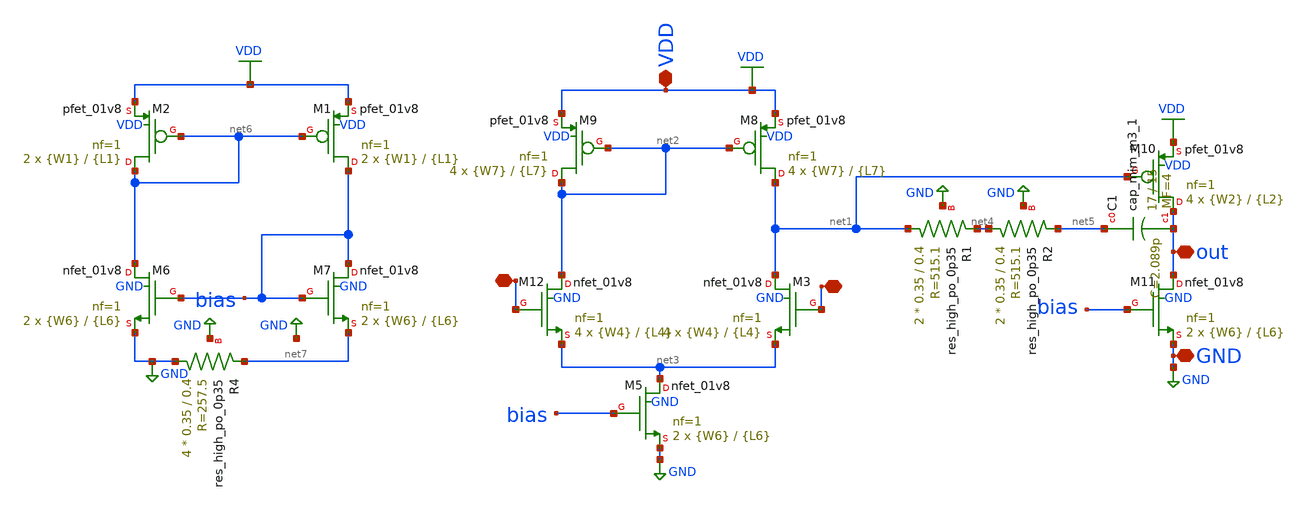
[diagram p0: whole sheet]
** sch_path: xschem/op5_sp.sch
**.subckt op5_sp GND - + VDD out
*.iopin GND
*.iopin -
*.iopin +
*.iopin VDD
*.iopin out
XM8 net1 net2 VDD VDD sky130_fd_pr__pfet_01v8 L={L7} W={W7} nf=1 ad='int((nf+1)/2) * W/nf * 0.29' as='int((nf+2)/2) * W/nf * 0.29'
+ pd='2*int((nf+1)/2) * (W/nf + 0.29)' ps='2*int((nf+2)/2) * (W/nf + 0.29)' nrd='0.29 / W' nrs='0.29 / W'
+ sa=0 sb=0 sd=0 mult=4 m=4
XM9 net2 net2 VDD VDD sky130_fd_pr__pfet_01v8 L={L7} W={W7} nf=1 ad='int((nf+1)/2) * W/nf * 0.29' as='int((nf+2)/2) * W/nf * 0.29'
+ pd='2*int((nf+1)/2) * (W/nf + 0.29)' ps='2*int((nf+2)/2) * (W/nf + 0.29)' nrd='0.29 / W' nrs='0.29 / W'
+ sa=0 sb=0 sd=0 mult=4 m=4
XM5 net3 bias GND GND sky130_fd_pr__nfet_01v8 L={L6} W={W6} nf=1 ad='int((nf+1)/2) * W/nf * 0.29' as='int((nf+2)/2) * W/nf * 0.29'
+ pd='2*int((nf+1)/2) * (W/nf + 0.29)' ps='2*int((nf+2)/2) * (W/nf + 0.29)' nrd='0.29 / W' nrs='0.29 / W'
+ sa=0 sb=0 sd=0 mult=2 m=2
XM10 out net1 VDD VDD sky130_fd_pr__pfet_01v8 L={L2} W={W2} nf=1 ad='int((nf+1)/2) * W/nf * 0.29' as='int((nf+2)/2) * W/nf * 0.29'
+ pd='2*int((nf+1)/2) * (W/nf + 0.29)' ps='2*int((nf+2)/2) * (W/nf + 0.29)' nrd='0.29 / W' nrs='0.29 / W'
+ sa=0 sb=0 sd=0 mult=4 m=4
XM11 out bias GND GND sky130_fd_pr__nfet_01v8 L={L6} W={W6} nf=1 ad='int((nf+1)/2) * W/nf * 0.29' as='int((nf+2)/2) * W/nf * 0.29'
+ pd='2*int((nf+1)/2) * (W/nf + 0.29)' ps='2*int((nf+2)/2) * (W/nf + 0.29)' nrd='0.29 / W' nrs='0.29 / W'
+ sa=0 sb=0 sd=0 mult=2 m=2
XC1 net5 out sky130_fd_pr__cap_mim_m3_1 W=17 L=15 MF=4 m=4
XR1 net1 net4 GND sky130_fd_pr__res_high_po_0p35 L=0.4 mult=2 m=2
XR2 net4 net5 GND sky130_fd_pr__res_high_po_0p35 L=0.4 mult=2 m=2
XM12 net2 - net3 GND sky130_fd_pr__nfet_01v8 L={L4} W={W4} nf=1 ad='int((nf+1)/2) * W/nf * 0.29' as='int((nf+2)/2) * W/nf * 0.29'
+ pd='2*int((nf+1)/2) * (W/nf + 0.29)' ps='2*int((nf+2)/2) * (W/nf + 0.29)' nrd='0.29 / W' nrs='0.29 / W'
+ sa=0 sb=0 sd=0 mult=4 m=4
XM3 net1 + net3 GND sky130_fd_pr__nfet_01v8 L={L4} W={W4} nf=1 ad='int((nf+1)/2) * W/nf * 0.29' as='int((nf+2)/2) * W/nf * 0.29'
+ pd='2*int((nf+1)/2) * (W/nf + 0.29)' ps='2*int((nf+2)/2) * (W/nf + 0.29)' nrd='0.29 / W' nrs='0.29 / W'
+ sa=0 sb=0 sd=0 mult=4 m=4
XM1 bias net6 VDD VDD sky130_fd_pr__pfet_01v8 L={L1} W={W1} nf=1 ad='int((nf+1)/2) * W/nf * 0.29' as='int((nf+2)/2) * W/nf * 0.29'
+ pd='2*int((nf+1)/2) * (W/nf + 0.29)' ps='2*int((nf+2)/2) * (W/nf + 0.29)' nrd='0.29 / W' nrs='0.29 / W'
+ sa=0 sb=0 sd=0 mult=2 m=2
XM2 net6 net6 VDD VDD sky130_fd_pr__pfet_01v8 L={L1} W={W1} nf=1 ad='int((nf+1)/2) * W/nf * 0.29' as='int((nf+2)/2) * W/nf * 0.29'
+ pd='2*int((nf+1)/2) * (W/nf + 0.29)' ps='2*int((nf+2)/2) * (W/nf + 0.29)' nrd='0.29 / W' nrs='0.29 / W'
+ sa=0 sb=0 sd=0 mult=2 m=2
XM6 net6 bias GND GND sky130_fd_pr__nfet_01v8 L={L6} W={W6} nf=1 ad='int((nf+1)/2) * W/nf * 0.29' as='int((nf+2)/2) * W/nf * 0.29'
+ pd='2*int((nf+1)/2) * (W/nf + 0.29)' ps='2*int((nf+2)/2) * (W/nf + 0.29)' nrd='0.29 / W' nrs='0.29 / W'
+ sa=0 sb=0 sd=0 mult=2 m=2
XM7 bias bias net7 GND sky130_fd_pr__nfet_01v8 L={L6} W={W6} nf=1 ad='int((nf+1)/2) * W/nf * 0.29' as='int((nf+2)/2) * W/nf * 0.29'
+ pd='2*int((nf+1)/2) * (W/nf + 0.29)' ps='2*int((nf+2)/2) * (W/nf + 0.29)' nrd='0.29 / W' nrs='0.29 / W'
+ sa=0 sb=0 sd=0 mult=2 m=2
XR4 GND net7 GND sky130_fd_pr__res_high_po_0p35 L=0.4 mult=4 m=4
**** begin user architecture code


**************
*PMOS cms
.param L1=20
.param W1=0.5

**************
*PMOS current differential
.param L7=10
.param W7=1

**************
*differential Pair
.param L4=10
.param W4=0.6

**************
*NMOS current control
.param L6=20
.param W6=1

**************
*Second Stage
.param L2=5
.param W2=1

**************
*NMOS current second stage
.param L3=10
.param W3=1

**************
*Current source Stage
.param L5=10
.param W5=1



**** end user architecture code
**.ends
.GLOBAL GND
.GLOBAL VDD
.end
